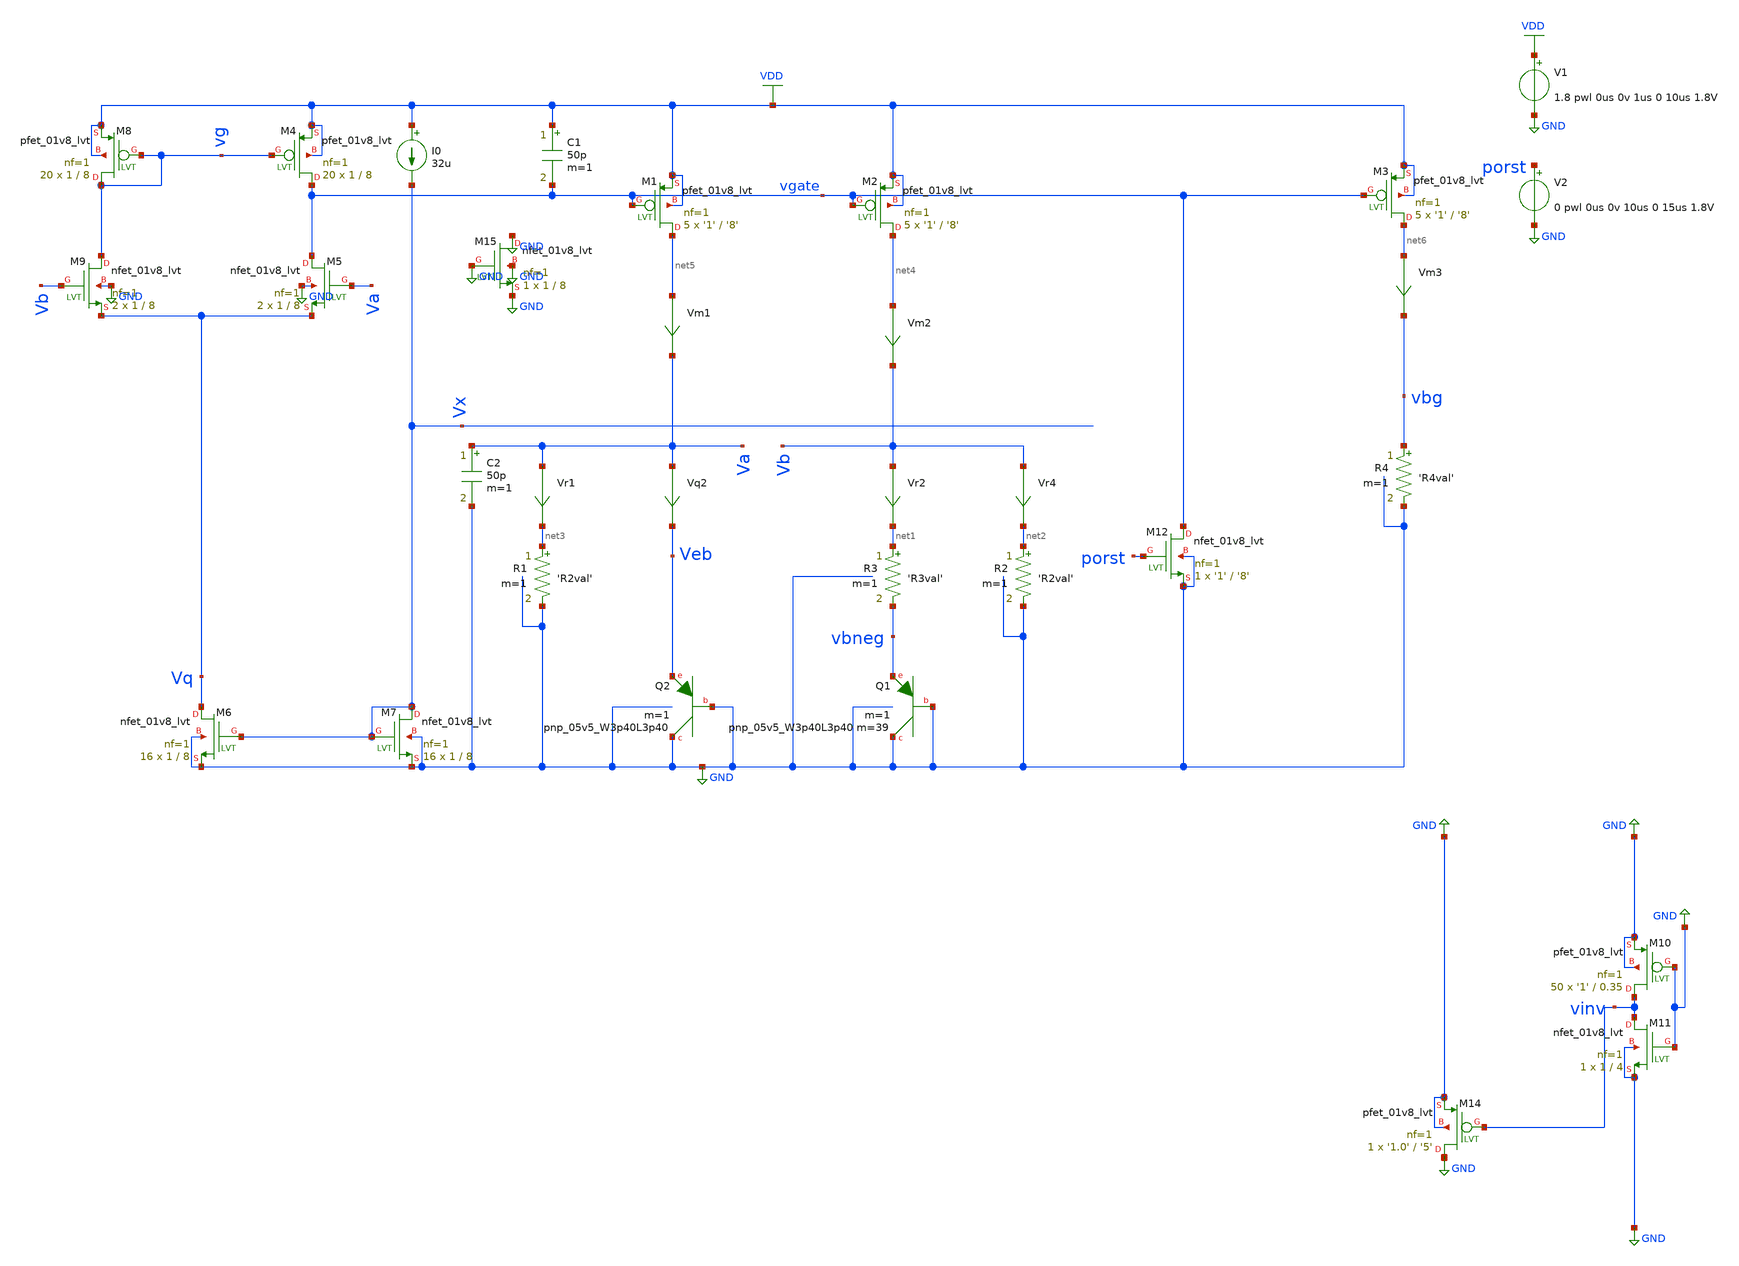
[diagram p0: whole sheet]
** sch_path: schematics/tsmc_bandgap_real_non_pdk_res.sch
**.subckt tsmc_bandgap_real_non_pdk_res
V1 VDD GND 1.8 pwl 0us 0v 1us 0 10us 1.8V
R3 net1 vbneg 'R3val' m=1
R4 vbg GND 'R4val' m=1
R1 net3 GND 'R2val' m=1
R2 net2 GND 'R2val' m=1
XQ2 GND GND Veb sky130_fd_pr__pnp_05v5_W3p40L3p40 m=1
Vr4 Vb net2 0
.save i(vr4)
Vr2 Vb net1 0
.save i(vr2)
Vm1 net5 Va 0
.save i(vm1)
Vm2 net4 Vb 0
.save i(vm2)
Vm3 net6 vbg 0
.save i(vm3)
Vr1 Va net3 0
.save i(vr1)
Vq2 Va Veb 0
.save i(vq2)
XQ1 GND GND vbneg sky130_fd_pr__pnp_05v5_W3p40L3p40 m=39 m=1
XM4 vgate vg VDD VDD sky130_fd_pr__pfet_01v8_lvt L=8 W=1 nf=1 ad='int((nf+1)/2) * W/nf * 0.29' as='int((nf+2)/2) * W/nf * 0.29'
+ pd='2*int((nf+1)/2) * (W/nf + 0.29)' ps='2*int((nf+2)/2) * (W/nf + 0.29)' nrd='0.29 / W' nrs='0.29 / W'
+ sa=0 sb=0 sd=0 mult=20 m=20
XM5 vgate Va Vq GND sky130_fd_pr__nfet_01v8_lvt L=8 W=1 nf=1 ad='int((nf+1)/2) * W/nf * 0.29' as='int((nf+2)/2) * W/nf * 0.29'
+ pd='2*int((nf+1)/2) * (W/nf + 0.29)' ps='2*int((nf+2)/2) * (W/nf + 0.29)' nrd='0.29 / W' nrs='0.29 / W'
+ sa=0 sb=0 sd=0 mult=2 m=2
XM6 Vq Vx GND GND sky130_fd_pr__nfet_01v8_lvt L=8 W=1 nf=1 ad='int((nf+1)/2) * W/nf * 0.29' as='int((nf+2)/2) * W/nf * 0.29'
+ pd='2*int((nf+1)/2) * (W/nf + 0.29)' ps='2*int((nf+2)/2) * (W/nf + 0.29)' nrd='0.29 / W' nrs='0.29 / W'
+ sa=0 sb=0 sd=0 mult=16 m=16
XM8 vg vg VDD VDD sky130_fd_pr__pfet_01v8_lvt L=8 W=1 nf=1 ad='int((nf+1)/2) * W/nf * 0.29' as='int((nf+2)/2) * W/nf * 0.29'
+ pd='2*int((nf+1)/2) * (W/nf + 0.29)' ps='2*int((nf+2)/2) * (W/nf + 0.29)' nrd='0.29 / W' nrs='0.29 / W'
+ sa=0 sb=0 sd=0 mult=20 m=20
XM9 vg Vb Vq GND sky130_fd_pr__nfet_01v8_lvt L=8 W=1 nf=1 ad='int((nf+1)/2) * W/nf * 0.29' as='int((nf+2)/2) * W/nf * 0.29'
+ pd='2*int((nf+1)/2) * (W/nf + 0.29)' ps='2*int((nf+2)/2) * (W/nf + 0.29)' nrd='0.29 / W' nrs='0.29 / W'
+ sa=0 sb=0 sd=0 mult=2 m=2
XM10 vinv GND GND GND sky130_fd_pr__pfet_01v8_lvt L=0.35 W='1' nf=1 ad='int((nf+1)/2) * W/nf * 0.29'
+ as='int((nf+2)/2) * W/nf * 0.29' pd='2*int((nf+1)/2) * (W/nf + 0.29)' ps='2*int((nf+2)/2) * (W/nf + 0.29)'
+ nrd='0.29 / W' nrs='0.29 / W' sa=0 sb=0 sd=0 mult=50 m=50
XM11 vinv GND GND GND sky130_fd_pr__nfet_01v8_lvt L=4 W=1 nf=1 ad='int((nf+1)/2) * W/nf * 0.29' as='int((nf+2)/2) * W/nf * 0.29'
+ pd='2*int((nf+1)/2) * (W/nf + 0.29)' ps='2*int((nf+2)/2) * (W/nf + 0.29)' nrd='0.29 / W' nrs='0.29 / W'
+ sa=0 sb=0 sd=0 mult=1 m=1
XM7 Vx Vx GND GND sky130_fd_pr__nfet_01v8_lvt L=8 W=1 nf=1 ad='int((nf+1)/2) * W/nf * 0.29' as='int((nf+2)/2) * W/nf * 0.29'
+ pd='2*int((nf+1)/2) * (W/nf + 0.29)' ps='2*int((nf+2)/2) * (W/nf + 0.29)' nrd='0.29 / W' nrs='0.29 / W'
+ sa=0 sb=0 sd=0 mult=16 m=16
C1 VDD vgate 50p m=1
C2 Va GND 50p m=1
XM1 net5 vgate VDD VDD sky130_fd_pr__pfet_01v8_lvt L='8' W='1' nf=1 ad='int((nf+1)/2) * W/nf * 0.29'
+ as='int((nf+2)/2) * W/nf * 0.29' pd='2*int((nf+1)/2) * (W/nf + 0.29)' ps='2*int((nf+2)/2) * (W/nf + 0.29)'
+ nrd='0.29 / W' nrs='0.29 / W' sa=0 sb=0 sd=0 mult=5 m=5
XM2 net4 vgate VDD VDD sky130_fd_pr__pfet_01v8_lvt L='8' W='1' nf=1 ad='int((nf+1)/2) * W/nf * 0.29'
+ as='int((nf+2)/2) * W/nf * 0.29' pd='2*int((nf+1)/2) * (W/nf + 0.29)' ps='2*int((nf+2)/2) * (W/nf + 0.29)'
+ nrd='0.29 / W' nrs='0.29 / W' sa=0 sb=0 sd=0 mult=5 m=5
XM3 net6 vgate VDD VDD sky130_fd_pr__pfet_01v8_lvt L='8' W='1' nf=1 ad='int((nf+1)/2) * W/nf * 0.29'
+ as='int((nf+2)/2) * W/nf * 0.29' pd='2*int((nf+1)/2) * (W/nf + 0.29)' ps='2*int((nf+2)/2) * (W/nf + 0.29)'
+ nrd='0.29 / W' nrs='0.29 / W' sa=0 sb=0 sd=0 mult=5 m=5
XM14 GND vinv GND GND sky130_fd_pr__pfet_01v8_lvt L='5' W='1.0' nf=1 ad='int((nf+1)/2) * W/nf * 0.29'
+ as='int((nf+2)/2) * W/nf * 0.29' pd='2*int((nf+1)/2) * (W/nf + 0.29)' ps='2*int((nf+2)/2) * (W/nf + 0.29)'
+ nrd='0.29 / W' nrs='0.29 / W' sa=0 sb=0 sd=0 mult=1 m=1
XM12 vgate porst GND GND sky130_fd_pr__nfet_01v8_lvt L='8' W='1' nf=1 ad='int((nf+1)/2) * W/nf * 0.29'
+ as='int((nf+2)/2) * W/nf * 0.29' pd='2*int((nf+1)/2) * (W/nf + 0.29)' ps='2*int((nf+2)/2) * (W/nf + 0.29)'
+ nrd='0.29 / W' nrs='0.29 / W' sa=0 sb=0 sd=0 mult=1 m=1
V2 porst GND 0 pwl 0us 0v 10us 0 15us 1.8V
XM15 GND GND GND GND sky130_fd_pr__nfet_01v8_lvt L=8 W=1 nf=1 ad='int((nf+1)/2) * W/nf * 0.29' as='int((nf+2)/2) * W/nf * 0.29'
+ pd='2*int((nf+1)/2) * (W/nf + 0.29)' ps='2*int((nf+2)/2) * (W/nf + 0.29)' nrd='0.29 / W' nrs='0.29 / W'
+ sa=0 sb=0 sd=0 mult=1 m=1
I0 VDD Vx 32u
**** begin user architecture code

.include $::SKYWATER_MODELS/cells/nfet_01v8/sky130_fd_pr__nfet_01v8__tt.corner.spice
.include $::SKYWATER_MODELS/cells/nfet_01v8_lvt/sky130_fd_pr__nfet_01v8_lvt__tt.corner.spice
.include $::SKYWATER_MODELS/cells/pfet_01v8/sky130_fd_pr__pfet_01v8__tt.corner.spice
.include $::SKYWATER_MODELS/cells/nfet_03v3_nvt/sky130_fd_pr__nfet_03v3_nvt__tt.corner.spice
.include $::SKYWATER_MODELS/cells/nfet_05v0_nvt/sky130_fd_pr__nfet_05v0_nvt__tt.corner.spice
.include $::SKYWATER_MODELS/cells/esd_nfet_01v8/sky130_fd_pr__esd_nfet_01v8__tt.corner.spice
.include $::SKYWATER_MODELS/cells/pfet_01v8_lvt/sky130_fd_pr__pfet_01v8_lvt__tt.corner.spice
.include $::SKYWATER_MODELS/cells/pfet_01v8_hvt/sky130_fd_pr__pfet_01v8_hvt__tt.corner.spice
.include $::SKYWATER_MODELS/cells/esd_pfet_g5v0d10v5/sky130_fd_pr__esd_pfet_g5v0d10v5__tt.corner.spice
.include $::SKYWATER_MODELS/cells/pfet_g5v0d10v5/sky130_fd_pr__pfet_g5v0d10v5__tt.corner.spice
.include $::SKYWATER_MODELS/cells/pfet_g5v0d16v0/sky130_fd_pr__pfet_g5v0d16v0__tt.corner.spice
.include $::SKYWATER_MODELS/cells/nfet_g5v0d10v5/sky130_fd_pr__nfet_g5v0d10v5__tt.corner.spice
.include $::SKYWATER_MODELS/cells/nfet_g5v0d16v0/sky130_fd_pr__nfet_g5v0d16v0__tt_discrete.corner.spice
.include $::SKYWATER_MODELS/cells/esd_nfet_g5v0d10v5/sky130_fd_pr__esd_nfet_g5v0d10v5__tt.corner.spice
.include $::SKYWATER_MODELS/models/corners/tt/nonfet.spice
* Mismatch parameters
.include $::SKYWATER_MODELS/cells/nfet_01v8/sky130_fd_pr__nfet_01v8__mismatch.corner.spice
.include $::SKYWATER_MODELS/cells/pfet_01v8/sky130_fd_pr__pfet_01v8__mismatch.corner.spice
.include $::SKYWATER_MODELS/cells/nfet_01v8_lvt/sky130_fd_pr__nfet_01v8_lvt__mismatch.corner.spice
.include $::SKYWATER_MODELS/cells/pfet_01v8_lvt/sky130_fd_pr__pfet_01v8_lvt__mismatch.corner.spice
.include $::SKYWATER_MODELS/cells/pfet_01v8_hvt/sky130_fd_pr__pfet_01v8_hvt__mismatch.corner.spice
.include $::SKYWATER_MODELS/cells/nfet_g5v0d10v5/sky130_fd_pr__nfet_g5v0d10v5__mismatch.corner.spice
.include $::SKYWATER_MODELS/cells/pfet_g5v0d10v5/sky130_fd_pr__pfet_g5v0d10v5__mismatch.corner.spice
.include $::SKYWATER_MODELS/cells/nfet_05v0_nvt/sky130_fd_pr__nfet_05v0_nvt__mismatch.corner.spice
.include $::SKYWATER_MODELS/cells/nfet_03v3_nvt/sky130_fd_pr__nfet_03v3_nvt__mismatch.corner.spice
* Resistor$::SKYWATER_MODELS/Capacitor
.include $::SKYWATER_MODELS/models/r+c/res_typical__cap_typical.spice
.include $::SKYWATER_MODELS/models/r+c/res_typical__cap_typical__lin.spice
* Special cells
.include $::SKYWATER_MODELS/models/corners/tt/specialized_cells.spice
* All models
.include $::SKYWATER_MODELS/models/all.spice
.include $::SKYWATER_MODELS/cells/pnp_05v5/sky130_fd_pr__pnp_05v5_W3p40L3p40.model.spice
* Corner
.include $::SKYWATER_MODELS/models/corners/tt/rf.spice



.option savecurrents
.param R3val='22.3751k'
.param alpha='1'
.param R2R3ratio='5.8366561*alpha'
.param R2val='R3val*R2R3ratio'
.param R4R2ratio='0.47810041'
.param R4val='R2val*R4R2ratio'
.control
save all  @m.xm1.msky130_fd_pr__pfet_01v8_lvt[gm]  @m.xm2.msky130_fd_pr__pfet_01v8_lvt[gm]
+  @m.xm3.msky130_fd_pr__pfet_01v8_lvt[gm]  @m.xm4.msky130_fd_pr__pfet_01v8_lvt[gm]  @m.xm5.msky130_fd_pr__nfet_01v8_lvt[gm]
+  @m.xm6.msky130_fd_pr__nfet_01v8_lvt[gm]  @m.xm7.msky130_fd_pr__nfet_01v8_lvt[gm]  @m.xm8.msky130_fd_pr__pfet_01v8_lvt[gm]
+  @m.xm9.msky130_fd_pr__nfet_01v8_lvt[gm]  @m.xm13.msky130_fd_pr__pfet_01v8_lvt[gm]

op
write tsmc_bandgap_real_non_pdk_res.raw
let id8=@m.xm8.msky130_fd_pr__pfet_01v8_lvt[id]
let id1=@m.xm1.msky130_fd_pr__pfet_01v8_lvt[id]
let vth5=@m.xm5.msky130_fd_pr__nfet_01v8_lvt[vth]
let vth6=@m.xm6.msky130_fd_pr__nfet_01v8_lvt[vth]
let wm8=@m.xm8.msky130_fd_pr__pfet_01v8_lvt[w]
let mm8=@m.xm8.msky130_fd_pr__pfet_01v8_lvt[m]
let weff8=wm8*mm8
let jd8=id8/weff8
let wm1=@m.xm1.msky130_fd_pr__pfet_01v8_lvt[w]
let mm1=@m.xm1.msky130_fd_pr__pfet_01v8_lvt[m]
let weff1=wm1*mm1
let jd1=id1/weff1
print vbg vgate vg va vb vx vinv vq
.endc


**** end user architecture code
**.ends
.GLOBAL VDD
.GLOBAL GND
.end
